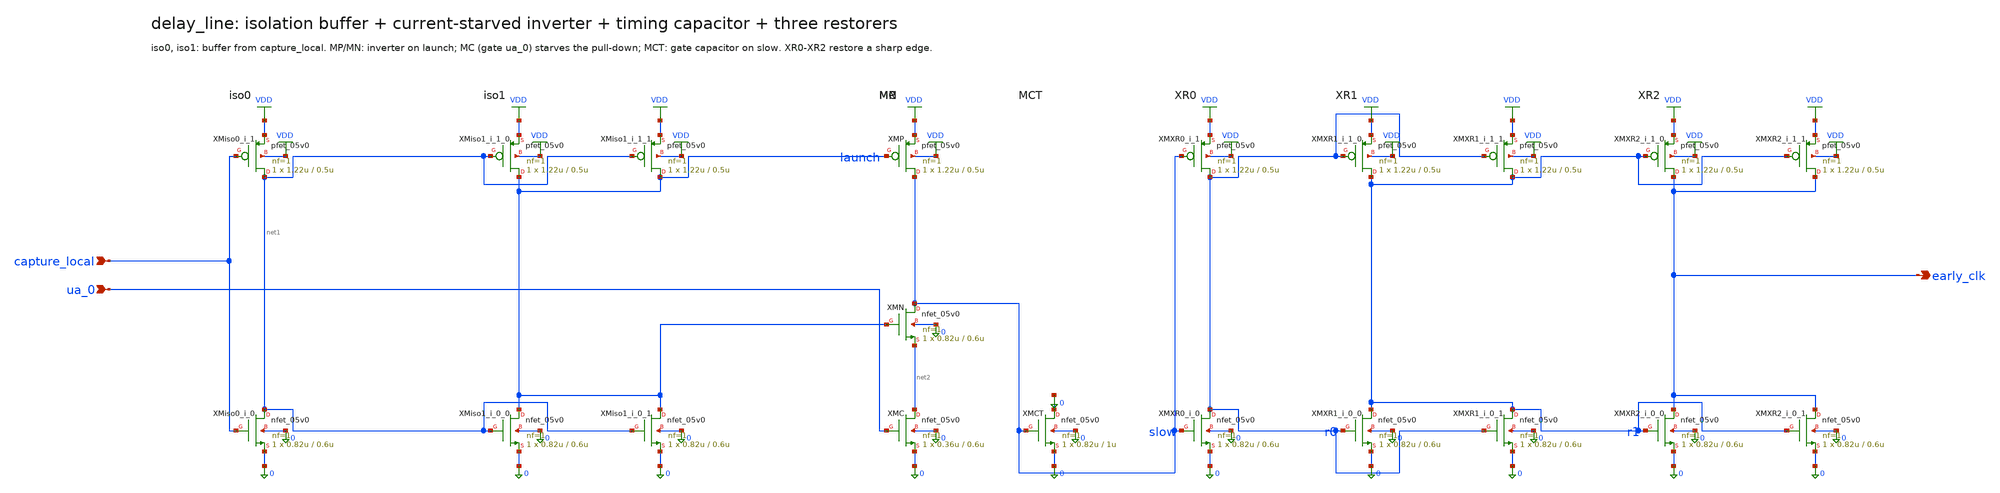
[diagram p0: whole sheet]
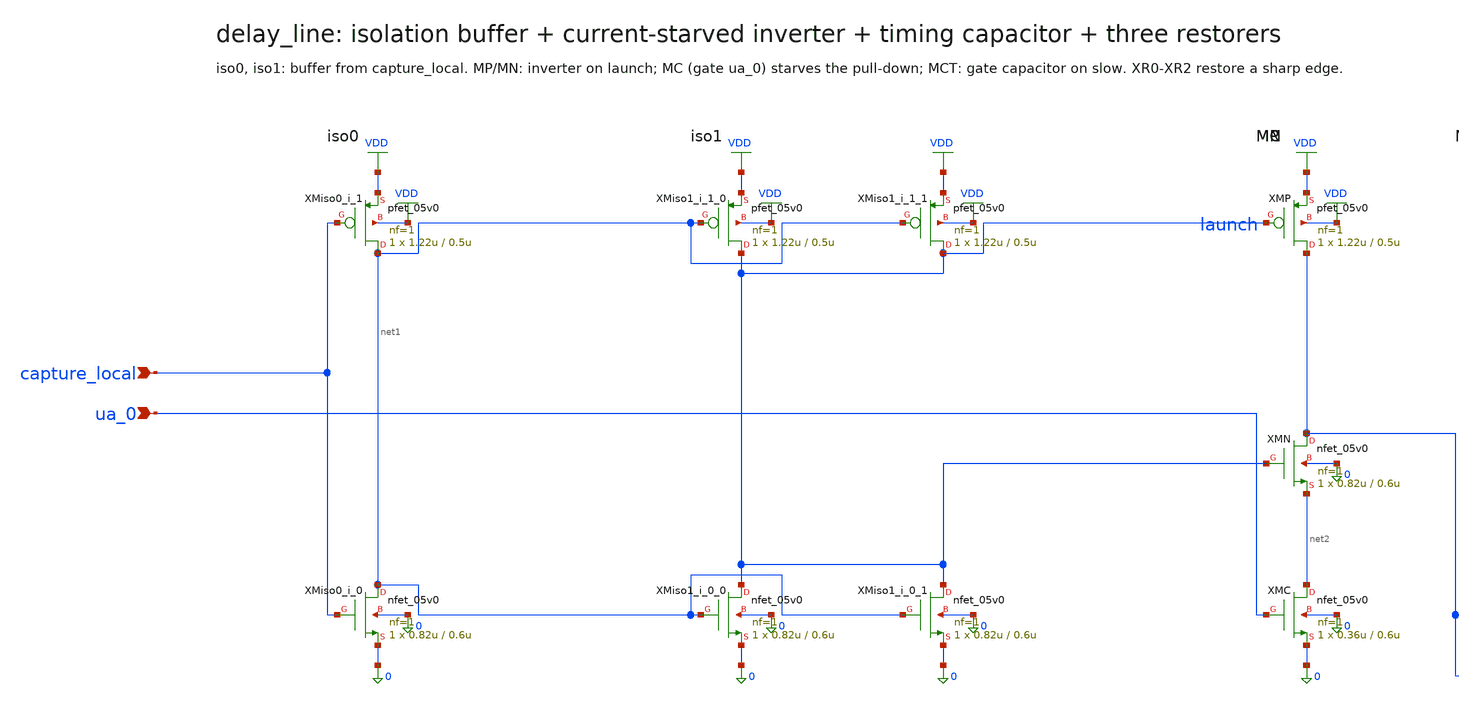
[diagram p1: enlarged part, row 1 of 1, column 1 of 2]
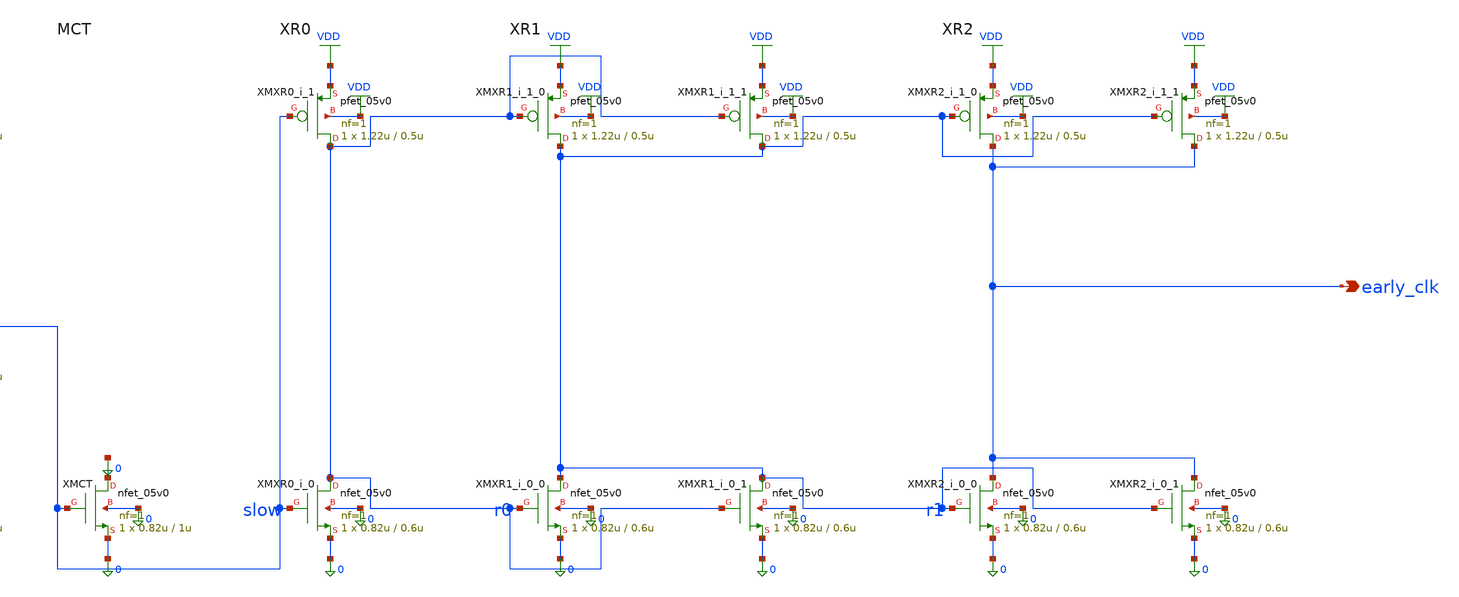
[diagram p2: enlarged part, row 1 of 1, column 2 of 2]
** sch_path: xschem/flat/delay_line.sch
**.subckt delay_line capture_local ua_0 early_clk
*.ipin capture_local
*.ipin ua_0
*.opin early_clk
XMiso0_i_0 net1 capture_local 0 0 nfet_05v0 L=0.6u W=0.82u nf=1 ad=4.1e-13 as=4.1e-13 pd=2.64e-06
+ ps=2.64e-06 nrd=0 nrs=0 sa=0 sb=0 sd=0 m=1
XMiso0_i_1 net1 capture_local VDD VDD pfet_05v0 L=0.5u W=1.22u nf=1 ad=6.1e-13 as=6.1e-13
+ pd=3.44e-06 ps=3.44e-06 nrd=0 nrs=0 sa=0 sb=0 sd=0 m=1
XMiso1_i_0_0 launch net1 0 0 nfet_05v0 L=0.6u W=0.82u nf=1 ad=4.1e-13 as=4.1e-13 pd=2.64e-06
+ ps=2.64e-06 nrd=0 nrs=0 sa=0 sb=0 sd=0 m=1
XMiso1_i_0_1 launch net1 0 0 nfet_05v0 L=0.6u W=0.82u nf=1 ad=4.1e-13 as=4.1e-13 pd=2.64e-06
+ ps=2.64e-06 nrd=0 nrs=0 sa=0 sb=0 sd=0 m=1
XMiso1_i_1_0 launch net1 VDD VDD pfet_05v0 L=0.5u W=1.22u nf=1 ad=6.1e-13 as=6.1e-13 pd=3.44e-06
+ ps=3.44e-06 nrd=0 nrs=0 sa=0 sb=0 sd=0 m=1
XMiso1_i_1_1 launch net1 VDD VDD pfet_05v0 L=0.5u W=1.22u nf=1 ad=6.1e-13 as=6.1e-13 pd=3.44e-06
+ ps=3.44e-06 nrd=0 nrs=0 sa=0 sb=0 sd=0 m=1
XMXR0_i_0 r0 slow 0 0 nfet_05v0 L=0.6u W=0.82u nf=1 ad=4.1e-13 as=4.1e-13 pd=2.64e-06 ps=2.64e-06
+ nrd=0 nrs=0 sa=0 sb=0 sd=0 m=1
XMXR0_i_1 r0 slow VDD VDD pfet_05v0 L=0.5u W=1.22u nf=1 ad=6.1e-13 as=6.1e-13 pd=3.44e-06
+ ps=3.44e-06 nrd=0 nrs=0 sa=0 sb=0 sd=0 m=1
XMXR1_i_0_0 r1 r0 0 0 nfet_05v0 L=0.6u W=0.82u nf=1 ad=4.1e-13 as=4.1e-13 pd=2.64e-06 ps=2.64e-06
+ nrd=0 nrs=0 sa=0 sb=0 sd=0 m=1
XMXR1_i_0_1 r1 r0 0 0 nfet_05v0 L=0.6u W=0.82u nf=1 ad=4.1e-13 as=4.1e-13 pd=2.64e-06 ps=2.64e-06
+ nrd=0 nrs=0 sa=0 sb=0 sd=0 m=1
XMXR1_i_1_0 r1 r0 VDD VDD pfet_05v0 L=0.5u W=1.22u nf=1 ad=6.1e-13 as=6.1e-13 pd=3.44e-06
+ ps=3.44e-06 nrd=0 nrs=0 sa=0 sb=0 sd=0 m=1
XMXR1_i_1_1 r1 r0 VDD VDD pfet_05v0 L=0.5u W=1.22u nf=1 ad=6.1e-13 as=6.1e-13 pd=3.44e-06
+ ps=3.44e-06 nrd=0 nrs=0 sa=0 sb=0 sd=0 m=1
XMXR2_i_0_0 early_clk r1 0 0 nfet_05v0 L=0.6u W=0.82u nf=1 ad=4.1e-13 as=4.1e-13 pd=2.64e-06
+ ps=2.64e-06 nrd=0 nrs=0 sa=0 sb=0 sd=0 m=1
XMXR2_i_0_1 early_clk r1 0 0 nfet_05v0 L=0.6u W=0.82u nf=1 ad=4.1e-13 as=4.1e-13 pd=2.64e-06
+ ps=2.64e-06 nrd=0 nrs=0 sa=0 sb=0 sd=0 m=1
XMXR2_i_1_0 early_clk r1 VDD VDD pfet_05v0 L=0.5u W=1.22u nf=1 ad=6.1e-13 as=6.1e-13 pd=3.44e-06
+ ps=3.44e-06 nrd=0 nrs=0 sa=0 sb=0 sd=0 m=1
XMXR2_i_1_1 early_clk r1 VDD VDD pfet_05v0 L=0.5u W=1.22u nf=1 ad=6.1e-13 as=6.1e-13 pd=3.44e-06
+ ps=3.44e-06 nrd=0 nrs=0 sa=0 sb=0 sd=0 m=1
XMP slow launch VDD VDD pfet_05v0 L=0.5u W=1.22u nf=1 ad=6.1e-13 as=6.1e-13 pd=3.44e-06 ps=3.44e-06
+ nrd=0 nrs=0 sa=0 sb=0 sd=0 m=1
XMN slow launch net2 0 nfet_05v0 L=0.6u W=0.82u nf=1 ad=4.1e-13 as=4.1e-13 pd=2.64e-06 ps=2.64e-06
+ nrd=0 nrs=0 sa=0 sb=0 sd=0 m=1
XMC net2 ua_0 0 0 nfet_05v0 L=0.6u W=0.36u nf=1 ad=1.8e-13 as=1.8e-13 pd=1.72e-06 ps=1.72e-06 nrd=0
+ nrs=0 sa=0 sb=0 sd=0 m=1
XMCT 0 slow 0 0 nfet_05v0 L=1u W=0.82u nf=1 ad=4.1e-13 as=4.1e-13 pd=2.64e-06 ps=2.64e-06 nrd=0
+ nrs=0 sa=0 sb=0 sd=0 m=1
**.ends
.GLOBAL VDD
.end
